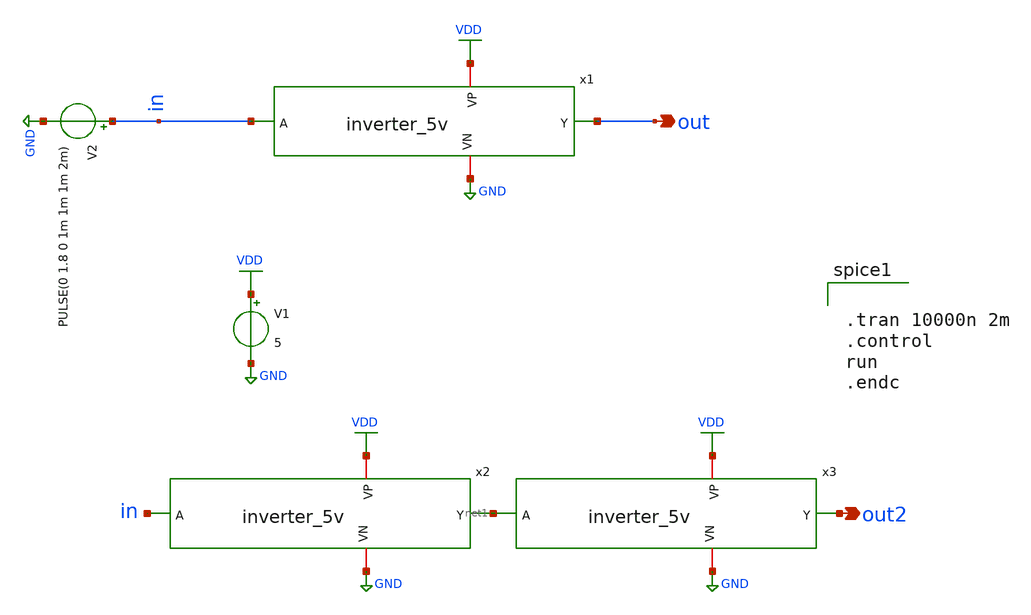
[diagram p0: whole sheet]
** sch_path: ADC/4bit_C2C/MagicAndSpice/inverter_5v_TB.sch
**.subckt inverter_5v_TB out out2
*.opin out
*.opin out2
x1 VDD in out GND inverter_5v
V1 VDD GND 5
V2 in GND PULSE(0 1.8 0 1m 1m 1m 2m)
x2 VDD in net1 GND inverter_5v
x3 VDD net1 out2 GND inverter_5v
**** begin user architecture code
 .lib $::SKYWATER_MODELS/sky130.lib.spice tt


.tran 10000n 2m
.control
run
.endc

**** end user architecture code
**.ends

* expanding   symbol:  /home/ee431/workspace/6SAR_CDAC/inverter_5v.sym # of pins=4
** sym_path: ADC/16bit_C2C/MagicAndSpice/inverter_5v.sym
** sch_path: ADC/16bit_C2C/MagicAndSpice/inverter_5v.sch
.subckt inverter_5v VP A Y VN
*.ipin A
*.opin Y
*.iopin VP
*.iopin VN
XM6 Y A VN VN sky130_fd_pr__nfet_g5v0d10v5 L=0.5 W=100 nf=1 ad='int((nf+1)/2) * W/nf * 0.29' as='int((nf+2)/2) * W/nf * 0.29'
+ pd='2*int((nf+1)/2) * (W/nf + 0.29)' ps='2*int((nf+2)/2) * (W/nf + 0.29)' nrd='0.29 / W' nrs='0.29 / W'
+ sa=0 sb=0 sd=0 mult=1 m=1
XM11 Y A VP VP sky130_fd_pr__pfet_g5v0d10v5 L=0.5 W=100 nf=1 ad='int((nf+1)/2) * W/nf * 0.29' as='int((nf+2)/2) * W/nf * 0.29'
+ pd='2*int((nf+1)/2) * (W/nf + 0.29)' ps='2*int((nf+2)/2) * (W/nf + 0.29)' nrd='0.29 / W' nrs='0.29 / W'
+ sa=0 sb=0 sd=0 mult=1 m=1
.ends

.GLOBAL GND
.GLOBAL VDD
.end
